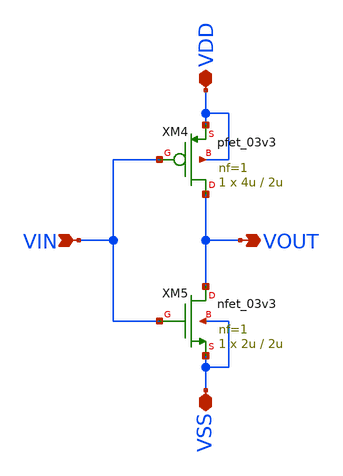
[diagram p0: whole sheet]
** sch_path: Clock_Generator_PAKISTAN_06/Xschem/strong_inv.sch
**.subckt strong_inv VDD VIN VOUT VSS
*.iopin VDD
*.ipin VIN
*.opin VOUT
*.iopin VSS
XM4 VOUT VIN VDD VDD pfet_03v3 L=2u W=4u nf=1 ad='int((nf+1)/2) * W/nf * 0.18u' as='int((nf+2)/2) * W/nf * 0.18u'
+ pd='2*int((nf+1)/2) * (W/nf + 0.18u)' ps='2*int((nf+2)/2) * (W/nf + 0.18u)' nrd='0.18u / W' nrs='0.18u / W'
+ sa=0 sb=0 sd=0 m=1
XM5 VOUT VIN VSS VSS nfet_03v3 L=2u W=2u nf=1 ad='int((nf+1)/2) * W/nf * 0.18u' as='int((nf+2)/2) * W/nf * 0.18u'
+ pd='2*int((nf+1)/2) * (W/nf + 0.18u)' ps='2*int((nf+2)/2) * (W/nf + 0.18u)' nrd='0.18u / W' nrs='0.18u / W'
+ sa=0 sb=0 sd=0 m=1
**.ends
.end
